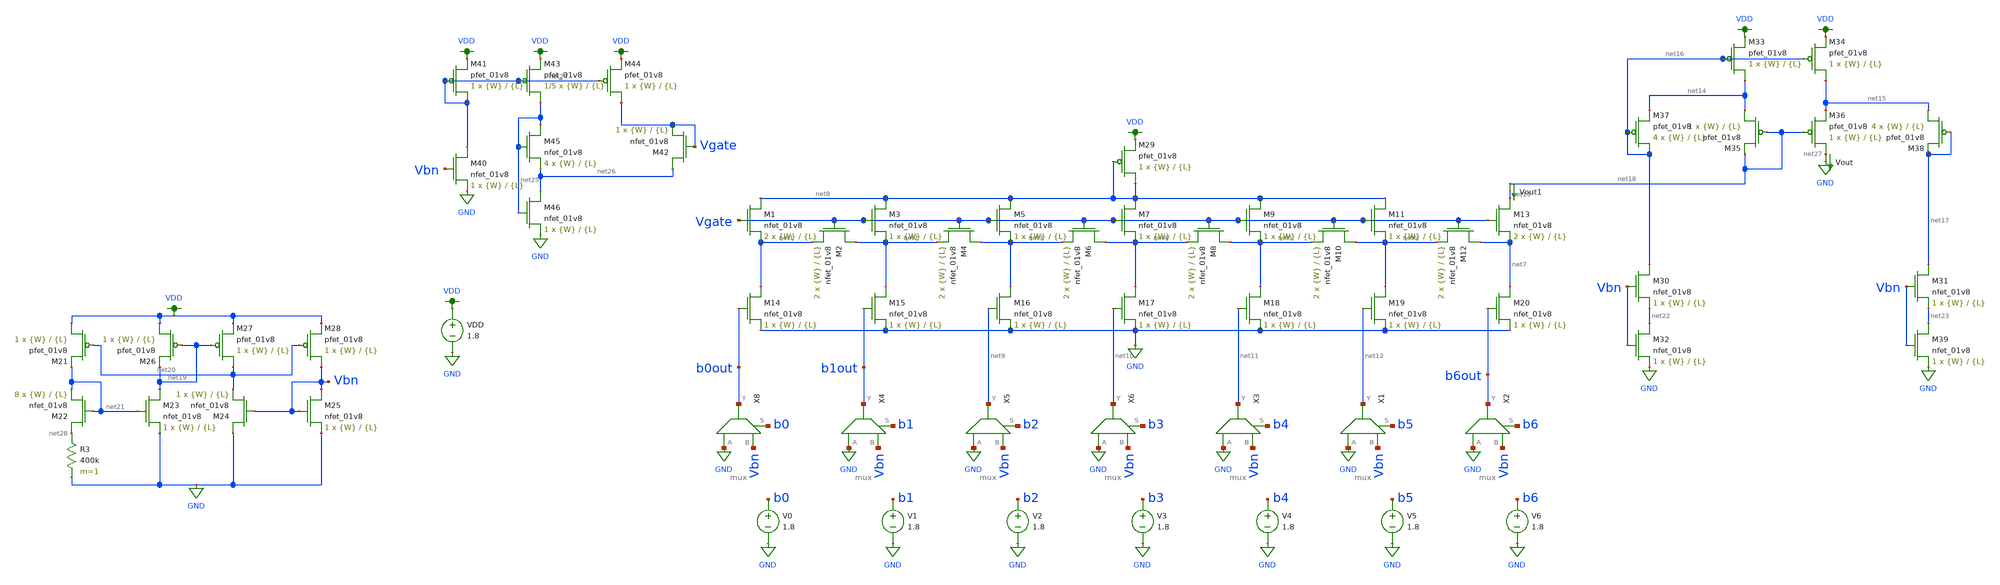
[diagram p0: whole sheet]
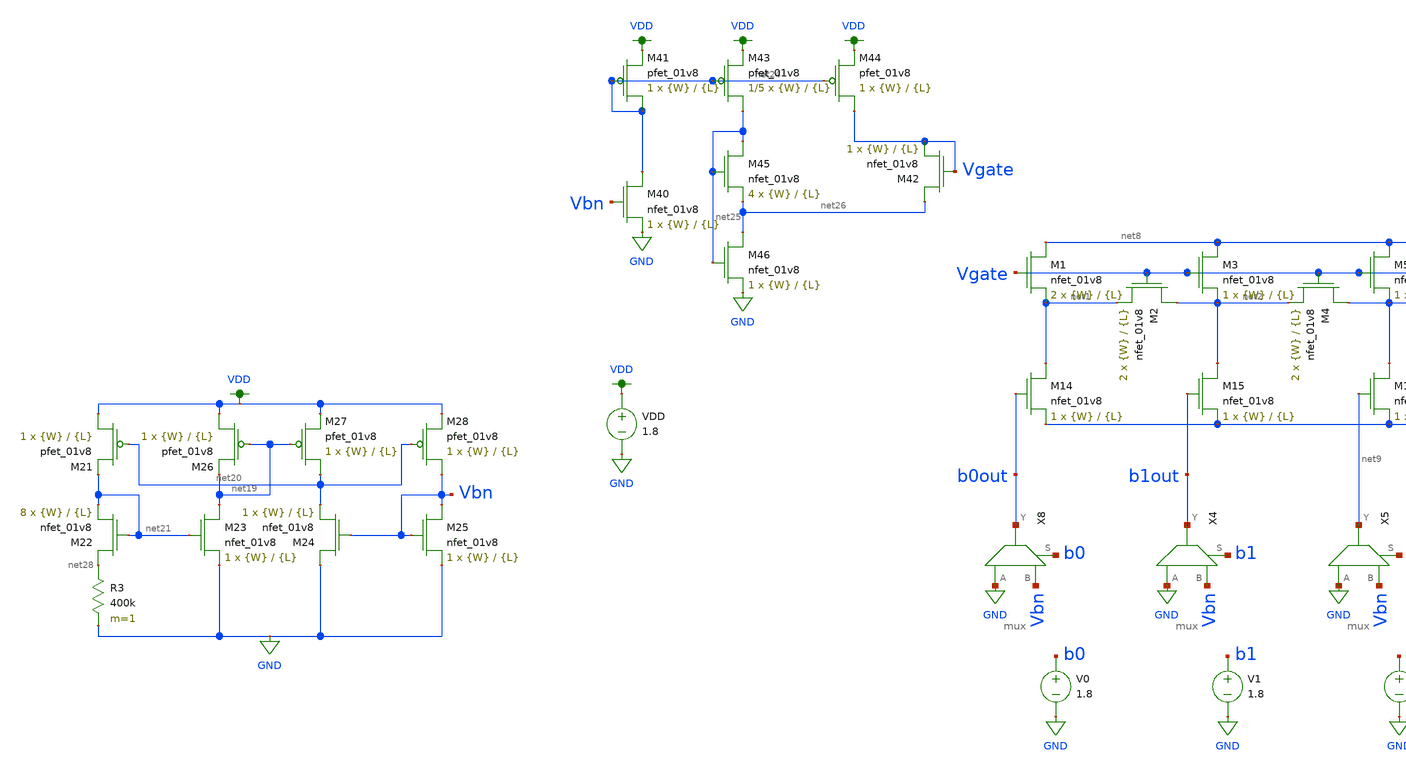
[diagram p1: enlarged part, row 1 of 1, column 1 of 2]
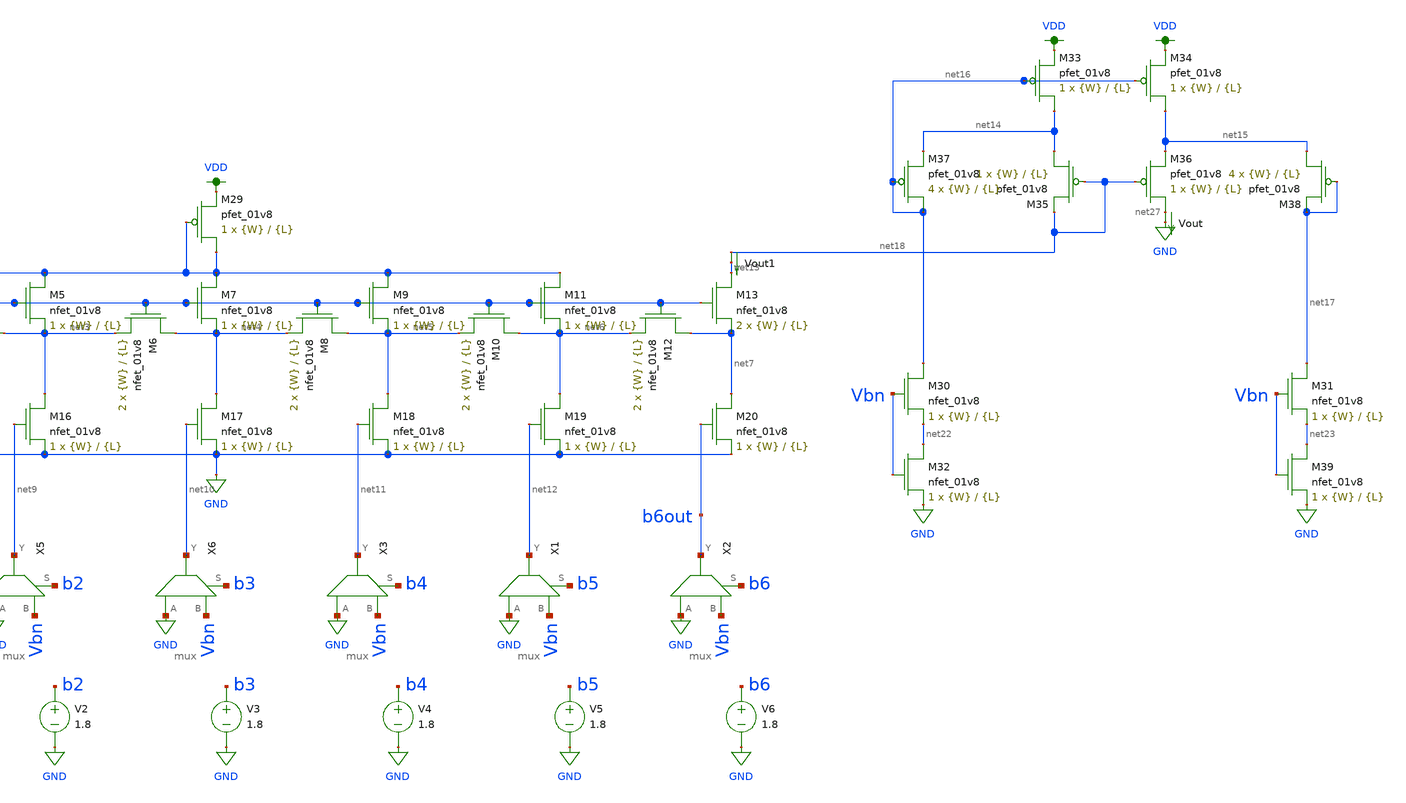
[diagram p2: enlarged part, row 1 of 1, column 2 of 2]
** sch_path: schematics/dac_dnl_inl_current_mirror.sch
**.subckt dac_dnl_inl_current_mirror
XM1 net8 Vgate net1 GND sky130_fd_pr__nfet_01v8 L={L} W={W} nf=1 ad='int((nf+1)/2) * W/nf * 0.29' as='int((nf+2)/2) * W/nf * 0.29'
+ pd='2*int((nf+1)/2) * (W/nf + 0.29)' ps='2*int((nf+2)/2) * (W/nf + 0.29)' nrd='0.29 / W' nrs='0.29 / W'
+ sa=0 sb=0 sd=0 mult=2 m=2
XM2 net2 Vgate net1 GND sky130_fd_pr__nfet_01v8 L={L} W={W} nf=1 ad='int((nf+1)/2) * W/nf * 0.29' as='int((nf+2)/2) * W/nf * 0.29'
+ pd='2*int((nf+1)/2) * (W/nf + 0.29)' ps='2*int((nf+2)/2) * (W/nf + 0.29)' nrd='0.29 / W' nrs='0.29 / W'
+ sa=0 sb=0 sd=0 mult=2 m=2
XM3 net8 Vgate net2 GND sky130_fd_pr__nfet_01v8 L={L} W={W} nf=1 ad='int((nf+1)/2) * W/nf * 0.29' as='int((nf+2)/2) * W/nf * 0.29'
+ pd='2*int((nf+1)/2) * (W/nf + 0.29)' ps='2*int((nf+2)/2) * (W/nf + 0.29)' nrd='0.29 / W' nrs='0.29 / W'
+ sa=0 sb=0 sd=0 mult=1 m=1
XM4 net3 Vgate net2 GND sky130_fd_pr__nfet_01v8 L={L} W={W} nf=1 ad='int((nf+1)/2) * W/nf * 0.29' as='int((nf+2)/2) * W/nf * 0.29'
+ pd='2*int((nf+1)/2) * (W/nf + 0.29)' ps='2*int((nf+2)/2) * (W/nf + 0.29)' nrd='0.29 / W' nrs='0.29 / W'
+ sa=0 sb=0 sd=0 mult=2 m=2
XM5 net8 Vgate net3 GND sky130_fd_pr__nfet_01v8 L={L} W={W} nf=1 ad='int((nf+1)/2) * W/nf * 0.29' as='int((nf+2)/2) * W/nf * 0.29'
+ pd='2*int((nf+1)/2) * (W/nf + 0.29)' ps='2*int((nf+2)/2) * (W/nf + 0.29)' nrd='0.29 / W' nrs='0.29 / W'
+ sa=0 sb=0 sd=0 mult=1 m=1
XM6 net4 Vgate net3 GND sky130_fd_pr__nfet_01v8 L={L} W={W} nf=1 ad='int((nf+1)/2) * W/nf * 0.29' as='int((nf+2)/2) * W/nf * 0.29'
+ pd='2*int((nf+1)/2) * (W/nf + 0.29)' ps='2*int((nf+2)/2) * (W/nf + 0.29)' nrd='0.29 / W' nrs='0.29 / W'
+ sa=0 sb=0 sd=0 mult=2 m=2
XM7 net8 Vgate net4 GND sky130_fd_pr__nfet_01v8 L={L} W={W} nf=1 ad='int((nf+1)/2) * W/nf * 0.29' as='int((nf+2)/2) * W/nf * 0.29'
+ pd='2*int((nf+1)/2) * (W/nf + 0.29)' ps='2*int((nf+2)/2) * (W/nf + 0.29)' nrd='0.29 / W' nrs='0.29 / W'
+ sa=0 sb=0 sd=0 mult=1 m=1
XM8 net5 Vgate net4 GND sky130_fd_pr__nfet_01v8 L={L} W={W} nf=1 ad='int((nf+1)/2) * W/nf * 0.29' as='int((nf+2)/2) * W/nf * 0.29'
+ pd='2*int((nf+1)/2) * (W/nf + 0.29)' ps='2*int((nf+2)/2) * (W/nf + 0.29)' nrd='0.29 / W' nrs='0.29 / W'
+ sa=0 sb=0 sd=0 mult=2 m=2
XM9 net8 Vgate net5 GND sky130_fd_pr__nfet_01v8 L={L} W={W} nf=1 ad='int((nf+1)/2) * W/nf * 0.29' as='int((nf+2)/2) * W/nf * 0.29'
+ pd='2*int((nf+1)/2) * (W/nf + 0.29)' ps='2*int((nf+2)/2) * (W/nf + 0.29)' nrd='0.29 / W' nrs='0.29 / W'
+ sa=0 sb=0 sd=0 mult=1 m=1
XM10 net6 Vgate net5 GND sky130_fd_pr__nfet_01v8 L={L} W={W} nf=1 ad='int((nf+1)/2) * W/nf * 0.29' as='int((nf+2)/2) * W/nf * 0.29'
+ pd='2*int((nf+1)/2) * (W/nf + 0.29)' ps='2*int((nf+2)/2) * (W/nf + 0.29)' nrd='0.29 / W' nrs='0.29 / W'
+ sa=0 sb=0 sd=0 mult=2 m=2
XM11 net8 Vgate net6 GND sky130_fd_pr__nfet_01v8 L={L} W={W} nf=1 ad='int((nf+1)/2) * W/nf * 0.29' as='int((nf+2)/2) * W/nf * 0.29'
+ pd='2*int((nf+1)/2) * (W/nf + 0.29)' ps='2*int((nf+2)/2) * (W/nf + 0.29)' nrd='0.29 / W' nrs='0.29 / W'
+ sa=0 sb=0 sd=0 mult=1 m=1
XM12 net7 Vgate net6 GND sky130_fd_pr__nfet_01v8 L={L} W={W} nf=1 ad='int((nf+1)/2) * W/nf * 0.29' as='int((nf+2)/2) * W/nf * 0.29'
+ pd='2*int((nf+1)/2) * (W/nf + 0.29)' ps='2*int((nf+2)/2) * (W/nf + 0.29)' nrd='0.29 / W' nrs='0.29 / W'
+ sa=0 sb=0 sd=0 mult=2 m=2
XM13 net13 Vgate net7 GND sky130_fd_pr__nfet_01v8 L={L} W={W} nf=1 ad='int((nf+1)/2) * W/nf * 0.29' as='int((nf+2)/2) * W/nf * 0.29'
+ pd='2*int((nf+1)/2) * (W/nf + 0.29)' ps='2*int((nf+2)/2) * (W/nf + 0.29)' nrd='0.29 / W' nrs='0.29 / W'
+ sa=0 sb=0 sd=0 mult=2 m=2
XM14 net1 b0out GND GND sky130_fd_pr__nfet_01v8 L={L} W={W} nf=1 ad='int((nf+1)/2) * W/nf * 0.29' as='int((nf+2)/2) * W/nf * 0.29'
+ pd='2*int((nf+1)/2) * (W/nf + 0.29)' ps='2*int((nf+2)/2) * (W/nf + 0.29)' nrd='0.29 / W' nrs='0.29 / W'
+ sa=0 sb=0 sd=0 mult=1 m=1
XM15 net2 b1out GND GND sky130_fd_pr__nfet_01v8 L={L} W={W} nf=1 ad='int((nf+1)/2) * W/nf * 0.29' as='int((nf+2)/2) * W/nf * 0.29'
+ pd='2*int((nf+1)/2) * (W/nf + 0.29)' ps='2*int((nf+2)/2) * (W/nf + 0.29)' nrd='0.29 / W' nrs='0.29 / W'
+ sa=0 sb=0 sd=0 mult=1 m=1
XM16 net3 net9 GND GND sky130_fd_pr__nfet_01v8 L={L} W={W} nf=1 ad='int((nf+1)/2) * W/nf * 0.29' as='int((nf+2)/2) * W/nf * 0.29'
+ pd='2*int((nf+1)/2) * (W/nf + 0.29)' ps='2*int((nf+2)/2) * (W/nf + 0.29)' nrd='0.29 / W' nrs='0.29 / W'
+ sa=0 sb=0 sd=0 mult=1 m=1
XM17 net4 net10 GND GND sky130_fd_pr__nfet_01v8 L={L} W={W} nf=1 ad='int((nf+1)/2) * W/nf * 0.29' as='int((nf+2)/2) * W/nf * 0.29'
+ pd='2*int((nf+1)/2) * (W/nf + 0.29)' ps='2*int((nf+2)/2) * (W/nf + 0.29)' nrd='0.29 / W' nrs='0.29 / W'
+ sa=0 sb=0 sd=0 mult=1 m=1
XM18 net5 net11 GND GND sky130_fd_pr__nfet_01v8 L={L} W={W} nf=1 ad='int((nf+1)/2) * W/nf * 0.29' as='int((nf+2)/2) * W/nf * 0.29'
+ pd='2*int((nf+1)/2) * (W/nf + 0.29)' ps='2*int((nf+2)/2) * (W/nf + 0.29)' nrd='0.29 / W' nrs='0.29 / W'
+ sa=0 sb=0 sd=0 mult=1 m=1
XM19 net6 net12 GND GND sky130_fd_pr__nfet_01v8 L={L} W={W} nf=1 ad='int((nf+1)/2) * W/nf * 0.29' as='int((nf+2)/2) * W/nf * 0.29'
+ pd='2*int((nf+1)/2) * (W/nf + 0.29)' ps='2*int((nf+2)/2) * (W/nf + 0.29)' nrd='0.29 / W' nrs='0.29 / W'
+ sa=0 sb=0 sd=0 mult=1 m=1
XM20 net7 b6out GND GND sky130_fd_pr__nfet_01v8 L={L} W={W} nf=1 ad='int((nf+1)/2) * W/nf * 0.29' as='int((nf+2)/2) * W/nf * 0.29'
+ pd='2*int((nf+1)/2) * (W/nf + 0.29)' ps='2*int((nf+2)/2) * (W/nf + 0.29)' nrd='0.29 / W' nrs='0.29 / W'
+ sa=0 sb=0 sd=0 mult=1 m=1
V0 b0 GND 1.8
V1 b1 GND 1.8
V2 b2 GND 1.8
V3 b3 GND 1.8
V4 b4 GND 1.8
V5 b5 GND 1.8
V6 b6 GND 1.8
Vout net27 GND 0
.save i(vout)
VDD VDD GND 1.8
XM33 net14 net16 VDD VDD sky130_fd_pr__pfet_01v8 L={L} W={W} nf=1 ad='int((nf+1)/2) * W/nf * 0.29' as='int((nf+2)/2) * W/nf * 0.29'
+ pd='2*int((nf+1)/2) * (W/nf + 0.29)' ps='2*int((nf+2)/2) * (W/nf + 0.29)' nrd='0.29 / W' nrs='0.29 / W'
+ sa=0 sb=0 sd=0 mult=1 m=1
XM34 net15 net16 VDD VDD sky130_fd_pr__pfet_01v8 L={L} W={W} nf=1 ad='int((nf+1)/2) * W/nf * 0.29' as='int((nf+2)/2) * W/nf * 0.29'
+ pd='2*int((nf+1)/2) * (W/nf + 0.29)' ps='2*int((nf+2)/2) * (W/nf + 0.29)' nrd='0.29 / W' nrs='0.29 / W'
+ sa=0 sb=0 sd=0 mult=1 m=1
XM35 net14 net18 net18 VDD sky130_fd_pr__pfet_01v8 L={L} W={W} nf=1 ad='int((nf+1)/2) * W/nf * 0.29'
+ as='int((nf+2)/2) * W/nf * 0.29' pd='2*int((nf+1)/2) * (W/nf + 0.29)' ps='2*int((nf+2)/2) * (W/nf + 0.29)'
+ nrd='0.29 / W' nrs='0.29 / W' sa=0 sb=0 sd=0 mult=1 m=1
XM36 net27 net18 net15 VDD sky130_fd_pr__pfet_01v8 L={L} W={W} nf=1 ad='int((nf+1)/2) * W/nf * 0.29'
+ as='int((nf+2)/2) * W/nf * 0.29' pd='2*int((nf+1)/2) * (W/nf + 0.29)' ps='2*int((nf+2)/2) * (W/nf + 0.29)'
+ nrd='0.29 / W' nrs='0.29 / W' sa=0 sb=0 sd=0 mult=1 m=1
XM37 net16 net16 net14 VDD sky130_fd_pr__pfet_01v8 L={L} W={W} nf=1 ad='int((nf+1)/2) * W/nf * 0.29'
+ as='int((nf+2)/2) * W/nf * 0.29' pd='2*int((nf+1)/2) * (W/nf + 0.29)' ps='2*int((nf+2)/2) * (W/nf + 0.29)'
+ nrd='0.29 / W' nrs='0.29 / W' sa=0 sb=0 sd=0 mult=4 m=4
XM38 net15 net17 net17 VDD sky130_fd_pr__pfet_01v8 L={L} W={W} nf=1 ad='int((nf+1)/2) * W/nf * 0.29'
+ as='int((nf+2)/2) * W/nf * 0.29' pd='2*int((nf+1)/2) * (W/nf + 0.29)' ps='2*int((nf+2)/2) * (W/nf + 0.29)'
+ nrd='0.29 / W' nrs='0.29 / W' sa=0 sb=0 sd=0 mult=4 m=4
XM21 VDD net20 net21 VDD sky130_fd_pr__pfet_01v8 L={L} W={W} nf=1 ad='int((nf+1)/2) * W/nf * 0.29' as='int((nf+2)/2) * W/nf * 0.29'
+ pd='2*int((nf+1)/2) * (W/nf + 0.29)' ps='2*int((nf+2)/2) * (W/nf + 0.29)' nrd='0.29 / W' nrs='0.29 / W'
+ sa=0 sb=0 sd=0 mult=1 m=1
XM22 net28 net21 net21 GND sky130_fd_pr__nfet_01v8 L={L} W={W} nf=1 ad='int((nf+1)/2) * W/nf * 0.29'
+ as='int((nf+2)/2) * W/nf * 0.29' pd='2*int((nf+1)/2) * (W/nf + 0.29)' ps='2*int((nf+2)/2) * (W/nf + 0.29)'
+ nrd='0.29 / W' nrs='0.29 / W' sa=0 sb=0 sd=0 mult=8 m=8
R3 net28 GND 400k m=1
XM23 net19 net21 GND GND sky130_fd_pr__nfet_01v8 L={L} W={W} nf=1 ad='int((nf+1)/2) * W/nf * 0.29' as='int((nf+2)/2) * W/nf * 0.29'
+ pd='2*int((nf+1)/2) * (W/nf + 0.29)' ps='2*int((nf+2)/2) * (W/nf + 0.29)' nrd='0.29 / W' nrs='0.29 / W'
+ sa=0 sb=0 sd=0 mult=1 m=1
XM24 GND Vbn net20 GND sky130_fd_pr__nfet_01v8 L={L} W={W} nf=1 ad='int((nf+1)/2) * W/nf * 0.29' as='int((nf+2)/2) * W/nf * 0.29'
+ pd='2*int((nf+1)/2) * (W/nf + 0.29)' ps='2*int((nf+2)/2) * (W/nf + 0.29)' nrd='0.29 / W' nrs='0.29 / W'
+ sa=0 sb=0 sd=0 mult=1 m=1
XM25 Vbn Vbn GND GND sky130_fd_pr__nfet_01v8 L={L} W={W} nf=1 ad='int((nf+1)/2) * W/nf * 0.29' as='int((nf+2)/2) * W/nf * 0.29'
+ pd='2*int((nf+1)/2) * (W/nf + 0.29)' ps='2*int((nf+2)/2) * (W/nf + 0.29)' nrd='0.29 / W' nrs='0.29 / W'
+ sa=0 sb=0 sd=0 mult=1 m=1
XM26 VDD net19 net19 VDD sky130_fd_pr__pfet_01v8 L={L} W={W} nf=1 ad='int((nf+1)/2) * W/nf * 0.29' as='int((nf+2)/2) * W/nf * 0.29'
+ pd='2*int((nf+1)/2) * (W/nf + 0.29)' ps='2*int((nf+2)/2) * (W/nf + 0.29)' nrd='0.29 / W' nrs='0.29 / W'
+ sa=0 sb=0 sd=0 mult=1 m=1
XM27 net20 net19 VDD VDD sky130_fd_pr__pfet_01v8 L={L} W={W} nf=1 ad='int((nf+1)/2) * W/nf * 0.29' as='int((nf+2)/2) * W/nf * 0.29'
+ pd='2*int((nf+1)/2) * (W/nf + 0.29)' ps='2*int((nf+2)/2) * (W/nf + 0.29)' nrd='0.29 / W' nrs='0.29 / W'
+ sa=0 sb=0 sd=0 mult=1 m=1
XM28 Vbn net20 VDD VDD sky130_fd_pr__pfet_01v8 L={L} W={W} nf=1 ad='int((nf+1)/2) * W/nf * 0.29' as='int((nf+2)/2) * W/nf * 0.29'
+ pd='2*int((nf+1)/2) * (W/nf + 0.29)' ps='2*int((nf+2)/2) * (W/nf + 0.29)' nrd='0.29 / W' nrs='0.29 / W'
+ sa=0 sb=0 sd=0 mult=1 m=1
XM29 net8 net8 VDD VDD sky130_fd_pr__pfet_01v8 L={L} W={W} nf=1 ad='int((nf+1)/2) * W/nf * 0.29' as='int((nf+2)/2) * W/nf * 0.29'
+ pd='2*int((nf+1)/2) * (W/nf + 0.29)' ps='2*int((nf+2)/2) * (W/nf + 0.29)' nrd='0.29 / W' nrs='0.29 / W'
+ sa=0 sb=0 sd=0 mult=1 m=1
XM30 net16 Vbn net22 GND sky130_fd_pr__nfet_01v8 L={L} W={W} nf=1 ad='int((nf+1)/2) * W/nf * 0.29' as='int((nf+2)/2) * W/nf * 0.29'
+ pd='2*int((nf+1)/2) * (W/nf + 0.29)' ps='2*int((nf+2)/2) * (W/nf + 0.29)' nrd='0.29 / W' nrs='0.29 / W'
+ sa=0 sb=0 sd=0 mult=1 m=1
XM31 net17 Vbn net23 GND sky130_fd_pr__nfet_01v8 L={L} W={W} nf=1 ad='int((nf+1)/2) * W/nf * 0.29' as='int((nf+2)/2) * W/nf * 0.29'
+ pd='2*int((nf+1)/2) * (W/nf + 0.29)' ps='2*int((nf+2)/2) * (W/nf + 0.29)' nrd='0.29 / W' nrs='0.29 / W'
+ sa=0 sb=0 sd=0 mult=1 m=1
XM32 net22 Vbn GND GND sky130_fd_pr__nfet_01v8 L={L} W={W} nf=1 ad='int((nf+1)/2) * W/nf * 0.29' as='int((nf+2)/2) * W/nf * 0.29'
+ pd='2*int((nf+1)/2) * (W/nf + 0.29)' ps='2*int((nf+2)/2) * (W/nf + 0.29)' nrd='0.29 / W' nrs='0.29 / W'
+ sa=0 sb=0 sd=0 mult=1 m=1
XM39 net23 Vbn GND GND sky130_fd_pr__nfet_01v8 L={L} W={W} nf=1 ad='int((nf+1)/2) * W/nf * 0.29' as='int((nf+2)/2) * W/nf * 0.29'
+ pd='2*int((nf+1)/2) * (W/nf + 0.29)' ps='2*int((nf+2)/2) * (W/nf + 0.29)' nrd='0.29 / W' nrs='0.29 / W'
+ sa=0 sb=0 sd=0 mult=1 m=1
X8 GND Vbn b0out b0 mux
X4 GND Vbn b1out b1 mux
X5 GND Vbn net9 b2 mux
X6 GND Vbn net10 b3 mux
X3 GND Vbn net11 b4 mux
X1 GND Vbn net12 b5 mux
X2 GND Vbn b6out b6 mux
Vout1 net18 net13 0
.save i(vout1)
XM40 net24 Vbn GND GND sky130_fd_pr__nfet_01v8 L={L} W={W} nf=1 ad='int((nf+1)/2) * W/nf * 0.29' as='int((nf+2)/2) * W/nf * 0.29'
+ pd='2*int((nf+1)/2) * (W/nf + 0.29)' ps='2*int((nf+2)/2) * (W/nf + 0.29)' nrd='0.29 / W' nrs='0.29 / W'
+ sa=0 sb=0 sd=0 mult=1 m=1
XM41 net24 net24 VDD VDD sky130_fd_pr__pfet_01v8 L={L} W={W} nf=1 ad='int((nf+1)/2) * W/nf * 0.29' as='int((nf+2)/2) * W/nf * 0.29'
+ pd='2*int((nf+1)/2) * (W/nf + 0.29)' ps='2*int((nf+2)/2) * (W/nf + 0.29)' nrd='0.29 / W' nrs='0.29 / W'
+ sa=0 sb=0 sd=0 mult=1 m=1
XM42 net26 Vgate Vgate GND sky130_fd_pr__nfet_01v8 L={L} W={W} nf=1 ad='int((nf+1)/2) * W/nf * 0.29'
+ as='int((nf+2)/2) * W/nf * 0.29' pd='2*int((nf+1)/2) * (W/nf + 0.29)' ps='2*int((nf+2)/2) * (W/nf + 0.29)'
+ nrd='0.29 / W' nrs='0.29 / W' sa=0 sb=0 sd=0 mult=1 m=1
XM43 net25 net24 VDD VDD sky130_fd_pr__pfet_01v8 L={L} W={W} nf=1 ad='int((nf+1)/2) * W/nf * 0.29' as='int((nf+2)/2) * W/nf * 0.29'
+ pd='2*int((nf+1)/2) * (W/nf + 0.29)' ps='2*int((nf+2)/2) * (W/nf + 0.29)' nrd='0.29 / W' nrs='0.29 / W'
+ sa=0 sb=0 sd=0 mult=1/5 m=1/5
XM44 Vgate net24 VDD VDD sky130_fd_pr__pfet_01v8 L={L} W={W} nf=1 ad='int((nf+1)/2) * W/nf * 0.29' as='int((nf+2)/2) * W/nf * 0.29'
+ pd='2*int((nf+1)/2) * (W/nf + 0.29)' ps='2*int((nf+2)/2) * (W/nf + 0.29)' nrd='0.29 / W' nrs='0.29 / W'
+ sa=0 sb=0 sd=0 mult=1 m=1
XM45 net25 net25 net26 GND sky130_fd_pr__nfet_01v8 L={L} W={W} nf=1 ad='int((nf+1)/2) * W/nf * 0.29'
+ as='int((nf+2)/2) * W/nf * 0.29' pd='2*int((nf+1)/2) * (W/nf + 0.29)' ps='2*int((nf+2)/2) * (W/nf + 0.29)'
+ nrd='0.29 / W' nrs='0.29 / W' sa=0 sb=0 sd=0 mult=4 m=4
XM46 net26 net25 GND GND sky130_fd_pr__nfet_01v8 L={L} W={W} nf=1 ad='int((nf+1)/2) * W/nf * 0.29' as='int((nf+2)/2) * W/nf * 0.29'
+ pd='2*int((nf+1)/2) * (W/nf + 0.29)' ps='2*int((nf+2)/2) * (W/nf + 0.29)' nrd='0.29 / W' nrs='0.29 / W'
+ sa=0 sb=0 sd=0 mult=1 m=1
**** begin user architecture code

.param W=1
.param L=4
.control
set wr_vecnames
set wr_singlescale
let code = 0
  while code < 128
    if code eq 0
      let b0 = 0
    else
      let b0 = code % 2 * 1.8
    end
    if floor(code / 2) eq 0
      let b1 = 0
    else
      let b1 = floor(code / 2) % 2 * 1.8
    end
    if floor(code / 4) eq 0
      let b2 = 0
    else
      let b2 = floor(code / 4) % 2 * 1.8
    end
    if floor(code / 8) eq 0
      let b3 = 0
    else
      let b3 = floor(code / 8) % 2 * 1.8
    end
    if floor(code / 16) eq 0
      let b4 = 0
    else
      let b4 = floor(code / 16) % 2 * 1.8
    end
    if floor(code / 32) eq 0
      let b5 = 0
    else
      let b5 = floor(code / 32) % 2 * 1.8
    end
    if floor(code / 64) eq 0
      let b6 = 0
    else
      let b6 = floor(code / 64) % 2 * 1.8
    end
    alter v0 $&b0
    alter v1 $&b1
    alter v2 $&b2
    alter v3 $&b3
    alter v4 $&b4
    alter v5 $&b5
    alter v6 $&b6
    save all
    op
    wrdata ~/Documents/current-output-dac-vlsi/simulations/dac_sim.txt v(Vbn) i(Vout) i(Vout1) v(b6)
+ v(b5) v(b4) v(b3) v(b2) v(b1) v(b0) v(b0out) v(b1out) v(b6out)
    if code eq 0
      set appendwrite
      set wr_vecnames = FALSE
    end
    let code = code + 1
  end
.endc


.option wnflag=1
.param MC_SWITCH=0.0
.lib ~/skywater/skywater-pdk/libraries/sky130_fd_pr_ngspice/latest/models/sky130.lib.spice tt

**** end user architecture code
**.ends

* expanding   symbol:  /home/madvlsi/Documents/current-output-dac-vlsi/schematics/mux.sym # of
*+ pins=4
** sym_path: /home/madvlsi/Documents/current-output-dac-vlsi/schematics/mux.sym
** sch_path: /home/madvlsi/Documents/current-output-dac-vlsi/schematics/mux.sch
.subckt mux A B Y S
*.ipin A
*.ipin B
*.ipin S
*.opin Y
XM1 A S Y VDD sky130_fd_pr__pfet_01v8 L=0.15 W=1 nf=1 ad='int((nf+1)/2) * W/nf * 0.29' as='int((nf+2)/2) * W/nf * 0.29'
+ pd='2*int((nf+1)/2) * (W/nf + 0.29)' ps='2*int((nf+2)/2) * (W/nf + 0.29)' nrd='0.29 / W' nrs='0.29 / W'
+ sa=0 sb=0 sd=0 mult=1 m=1
XM3 net1 S VDD VDD sky130_fd_pr__pfet_01v8 L=0.15 W=1 nf=1 ad='int((nf+1)/2) * W/nf * 0.29' as='int((nf+2)/2) * W/nf * 0.29'
+ pd='2*int((nf+1)/2) * (W/nf + 0.29)' ps='2*int((nf+2)/2) * (W/nf + 0.29)' nrd='0.29 / W' nrs='0.29 / W'
+ sa=0 sb=0 sd=0 mult=1 m=1
XM4 net1 S GND GND sky130_fd_pr__nfet_01v8 L=0.15 W=1 nf=1 ad='int((nf+1)/2) * W/nf * 0.29' as='int((nf+2)/2) * W/nf * 0.29'
+ pd='2*int((nf+1)/2) * (W/nf + 0.29)' ps='2*int((nf+2)/2) * (W/nf + 0.29)' nrd='0.29 / W' nrs='0.29 / W'
+ sa=0 sb=0 sd=0 mult=1 m=1
XM5 A net1 Y GND sky130_fd_pr__nfet_01v8 L=0.15 W=1 nf=1 ad='int((nf+1)/2) * W/nf * 0.29' as='int((nf+2)/2) * W/nf * 0.29'
+ pd='2*int((nf+1)/2) * (W/nf + 0.29)' ps='2*int((nf+2)/2) * (W/nf + 0.29)' nrd='0.29 / W' nrs='0.29 / W'
+ sa=0 sb=0 sd=0 mult=1 m=1
XM2 B net1 Y VDD sky130_fd_pr__pfet_01v8 L=0.15 W=1 nf=1 ad='int((nf+1)/2) * W/nf * 0.29' as='int((nf+2)/2) * W/nf * 0.29'
+ pd='2*int((nf+1)/2) * (W/nf + 0.29)' ps='2*int((nf+2)/2) * (W/nf + 0.29)' nrd='0.29 / W' nrs='0.29 / W'
+ sa=0 sb=0 sd=0 mult=1 m=1
XM6 B S Y GND sky130_fd_pr__nfet_01v8 L=0.15 W=1 nf=1 ad='int((nf+1)/2) * W/nf * 0.29' as='int((nf+2)/2) * W/nf * 0.29'
+ pd='2*int((nf+1)/2) * (W/nf + 0.29)' ps='2*int((nf+2)/2) * (W/nf + 0.29)' nrd='0.29 / W' nrs='0.29 / W'
+ sa=0 sb=0 sd=0 mult=1 m=1
.ends

.GLOBAL GND
.GLOBAL VDD
.end
